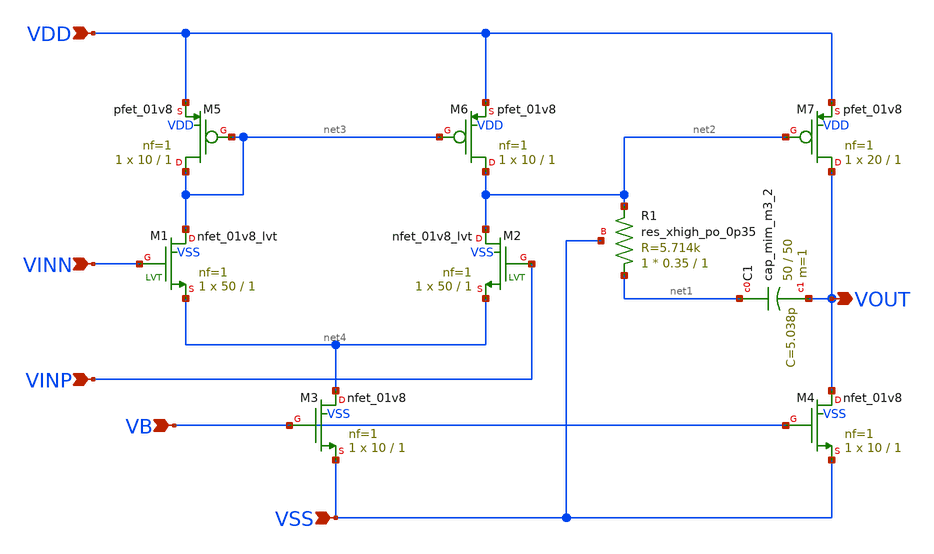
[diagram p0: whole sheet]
** sch_path: xschem/RF_amp.sch
**.subckt RF_amp VDD VINN VINP VB VSS VOUT
*.ipin VDD
*.ipin VINN
*.ipin VINP
*.ipin VB
*.ipin VSS
*.opin VOUT
XM1 net3 VINN net4 VSS sky130_fd_pr__nfet_01v8_lvt L=1 W=50 nf=1 ad='int((nf+1)/2) * W/nf * 0.29' as='int((nf+2)/2) * W/nf * 0.29'
+ pd='2*int((nf+1)/2) * (W/nf + 0.29)' ps='2*int((nf+2)/2) * (W/nf + 0.29)' nrd='0.29 / W' nrs='0.29 / W'
+ sa=0 sb=0 sd=0 mult=1 m=1
XM2 net2 VINP net4 VSS sky130_fd_pr__nfet_01v8_lvt L=1 W=50 nf=1 ad='int((nf+1)/2) * W/nf * 0.29' as='int((nf+2)/2) * W/nf * 0.29'
+ pd='2*int((nf+1)/2) * (W/nf + 0.29)' ps='2*int((nf+2)/2) * (W/nf + 0.29)' nrd='0.29 / W' nrs='0.29 / W'
+ sa=0 sb=0 sd=0 mult=1 m=1
XM5 net3 net3 VDD VDD sky130_fd_pr__pfet_01v8 L=1 W=10 nf=1 ad='int((nf+1)/2) * W/nf * 0.29' as='int((nf+2)/2) * W/nf * 0.29'
+ pd='2*int((nf+1)/2) * (W/nf + 0.29)' ps='2*int((nf+2)/2) * (W/nf + 0.29)' nrd='0.29 / W' nrs='0.29 / W'
+ sa=0 sb=0 sd=0 mult=1 m=1
XM6 net2 net3 VDD VDD sky130_fd_pr__pfet_01v8 L=1 W=10 nf=1 ad='int((nf+1)/2) * W/nf * 0.29' as='int((nf+2)/2) * W/nf * 0.29'
+ pd='2*int((nf+1)/2) * (W/nf + 0.29)' ps='2*int((nf+2)/2) * (W/nf + 0.29)' nrd='0.29 / W' nrs='0.29 / W'
+ sa=0 sb=0 sd=0 mult=1 m=1
XM7 VOUT net2 VDD VDD sky130_fd_pr__pfet_01v8 L=1 W=20 nf=1 ad='int((nf+1)/2) * W/nf * 0.29' as='int((nf+2)/2) * W/nf * 0.29'
+ pd='2*int((nf+1)/2) * (W/nf + 0.29)' ps='2*int((nf+2)/2) * (W/nf + 0.29)' nrd='0.29 / W' nrs='0.29 / W'
+ sa=0 sb=0 sd=0 mult=1 m=1
XR1 net1 net2 VSS sky130_fd_pr__res_xhigh_po_0p35 L=1 mult=1 m=1
XC1 net1 VOUT sky130_fd_pr__cap_mim_m3_2 W=50 L=50 MF=1 m=1
XM3 net4 VB VSS VSS sky130_fd_pr__nfet_01v8 L=1 W=10 nf=1 ad='int((nf+1)/2) * W/nf * 0.29' as='int((nf+2)/2) * W/nf * 0.29'
+ pd='2*int((nf+1)/2) * (W/nf + 0.29)' ps='2*int((nf+2)/2) * (W/nf + 0.29)' nrd='0.29 / W' nrs='0.29 / W'
+ sa=0 sb=0 sd=0 mult=1 m=1
XM4 VOUT VB VSS VSS sky130_fd_pr__nfet_01v8 L=1 W=10 nf=1 ad='int((nf+1)/2) * W/nf * 0.29' as='int((nf+2)/2) * W/nf * 0.29'
+ pd='2*int((nf+1)/2) * (W/nf + 0.29)' ps='2*int((nf+2)/2) * (W/nf + 0.29)' nrd='0.29 / W' nrs='0.29 / W'
+ sa=0 sb=0 sd=0 mult=1 m=1
**.ends
.end
